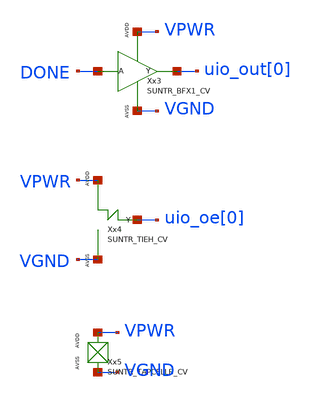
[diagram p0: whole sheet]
** sch_path: ip/tt06_sar_sky130nm/design/TT06_SAR_SKY130NM/tt_um_TT06_SAR_done.sch
**.subckt tt_um_TT06_SAR_done
Xx5 VPWR VGND SUNTR_TAPCELLB_CV xoffset=0 yoffset=0 angle=0
**.ends
.end
